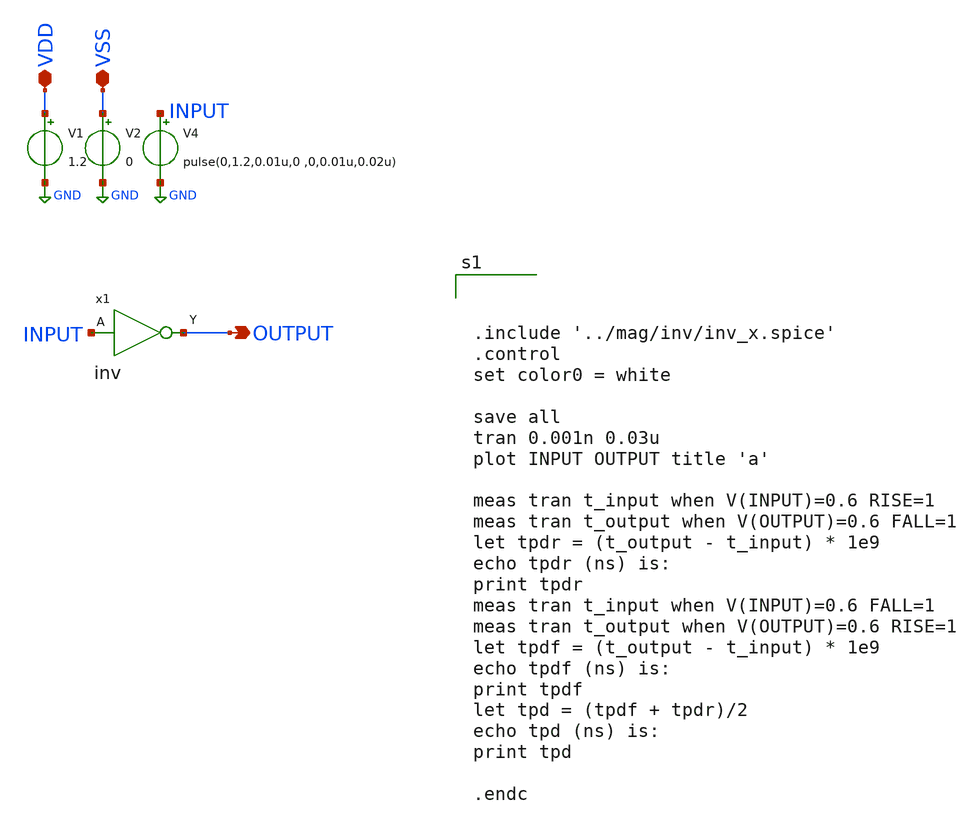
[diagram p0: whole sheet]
** sch_path: design/xschem/From Layout/INV/inv_TB.sch
**.subckt inv_TB OUTPUT VSS VDD
*.opin OUTPUT
*.iopin VSS
*.iopin VDD
V1 VDD GND 1.2
V2 VSS GND 0
V4 INPUT GND pulse(0,1.2,0.01u,0 ,0,0.01u,0.02u)
x1 INPUT VSS VDD OUTPUT inv
**** begin user architecture code

** opencircuitdesign pdks install
.lib $::SKYWATER_MODELS/sky130.lib.spice tt_mm





.include '../mag/inv/inv_x.spice'
.control
set color0 = white

save all
tran 0.001n 0.03u
plot INPUT OUTPUT title 'a'

meas tran t_input when V(INPUT)=0.6 RISE=1
meas tran t_output when V(OUTPUT)=0.6 FALL=1
let tpdr = (t_output - t_input) * 1e9
echo tpdr (ns) is:
print tpdr
meas tran t_input when V(INPUT)=0.6 FALL=1
meas tran t_output when V(OUTPUT)=0.6 RISE=1
let tpdf = (t_output - t_input) * 1e9
echo tpdf (ns) is:
print tpdf
let tpd = (tpdf + tpdr)/2
echo tpd (ns) is:
print tpd

.endc


**** end user architecture code
**.ends
.GLOBAL GND
.end
